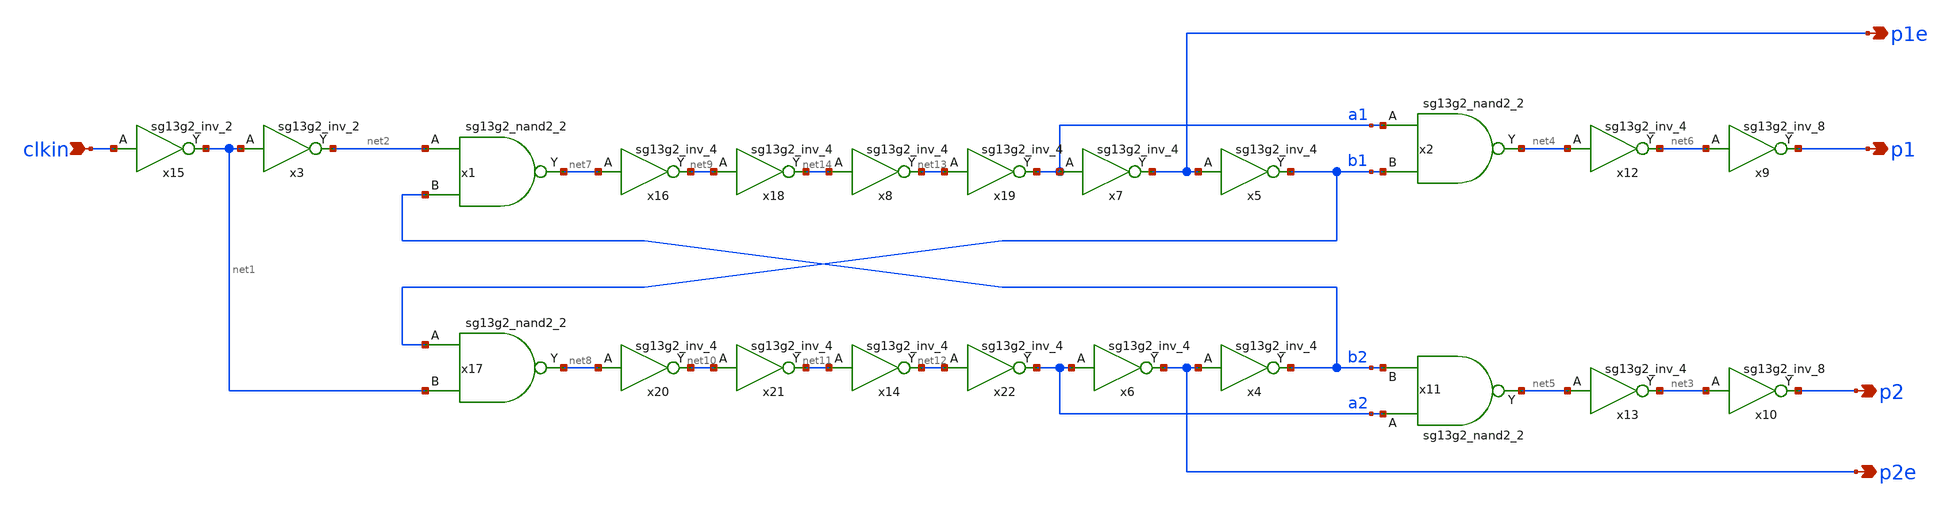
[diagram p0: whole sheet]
** sch_path: 5_Design/4_Layout/Team 4/xschem/clkgen_team4.sch
* IHP-GmbH/IHP-Open-PDK/ihp-sg13g2/libs.tech/xschem/sg13g2_stdcells/sg13g2_inv_2.sch:
* Copyright 2023 IHP PDK Authors
* Licensed under the Apache License, Version 2.0 (the "License");
**.subckt clkgen_team4 p1e p1 p2 p2e clkin
*.opin p1e
*.opin p1
*.opin p2
*.opin p2e
*.ipin clkin
x15 net1 clkin VDD VSS sg13g2_inv_2
x3 net2 net1 VDD VSS sg13g2_inv_2
x17 net8 b1 net1 VDD VSS sg13g2_nand2_2
x1 net7 net2 b2 VDD VSS sg13g2_nand2_2
x2 net4 a1 b1 VDD VSS sg13g2_nand2_2
x11 net5 a2 b2 VDD VSS sg13g2_nand2_2
x12 net6 net4 VDD VSS sg13g2_inv_4
x13 net3 net5 VDD VSS sg13g2_inv_4
x6 p2e a2 VDD VSS sg13g2_inv_4
x4 b2 p2e VDD VSS sg13g2_inv_4
x5 b1 p1e VDD VSS sg13g2_inv_4
x7 p1e a1 VDD VSS sg13g2_inv_4
x8 net13 net14 VDD VSS sg13g2_inv_4
x16 net9 net7 VDD VSS sg13g2_inv_4
x18 net14 net9 VDD VSS sg13g2_inv_4
x19 a1 net13 VDD VSS sg13g2_inv_4
x14 net12 net11 VDD VSS sg13g2_inv_4
x20 net10 net8 VDD VSS sg13g2_inv_4
x21 net11 net10 VDD VSS sg13g2_inv_4
x22 a2 net12 VDD VSS sg13g2_inv_4
x9 p1 net6 VDD VSS sg13g2_inv_8
x10 p2 net3 VDD VSS sg13g2_inv_8
**** begin user architecture code


.param temp=27 vdd=1.2 per=20n
.option method=gear2

.control
save all
tran 10p 15n
set color0=white
plot p1 p2
.endc



.lib /foss/pdks/sg13g2/libs.tech/ngspice/models/cornerMOSlv.lib mos_tt
.lib /foss/pdks/sg13g2/libs.tech/ngspice/models/cornerRES.lib res_typ
.inc /foss/pdks/sg13g2/libs.ref/sg13g2_stdcell/spice/sg13g2_stdcell.spice

**** end user architecture code
**.ends

* expanding   symbol:  sg13g2_stdcells/sg13g2_inv_2.sym # of pins=2
** sym_path: sg13g2_stdcells/sg13g2_inv_2.sym
** sch_path: sg13g2_stdcells/sg13g2_inv_2.sch
.subckt sg13g2_inv_2 Y A VDD VSS
*.opin Y
*.ipin A
*.iopin VDD
*.iopin VSS
XM1 Y A VSS VSS sg13_lv_nmos w=1.48u l=130.00n ng=2 m=1 mm_ok=1
XM2 Y A VDD VDD sg13_lv_pmos w=2.24u l=130.00n ng=2 m=1 mm_ok=1
.ends


* expanding   symbol:  sg13g2_stdcells/sg13g2_nand2_2.sym # of pins=3
** sym_path: sg13g2_stdcells/sg13g2_nand2_2.sym
** sch_path: sg13g2_stdcells/sg13g2_nand2_2.sch
.subckt sg13g2_nand2_2 Y A B VDD VSS
*.iopin VDD
*.iopin VSS
*.opin Y
*.ipin B
*.ipin A
XM1 Y A net1 VSS sg13_lv_nmos w=1.44u l=130.00n ng=2 m=1 mm_ok=1
XM2 net1 B VSS VSS sg13_lv_nmos w=1.44u l=130.00n ng=2 m=1 mm_ok=1
XM3 Y A VDD VDD sg13_lv_pmos w=2.24u l=130.00n ng=2 m=1 mm_ok=1
XM4 Y B VDD VDD sg13_lv_pmos w=2.24u l=130.00n ng=2 m=1 mm_ok=1
.ends


* expanding   symbol:  sg13g2_stdcells/sg13g2_inv_4.sym # of pins=2
** sym_path: sg13g2_stdcells/sg13g2_inv_4.sym
** sch_path: sg13g2_stdcells/sg13g2_inv_4.sch
.subckt sg13g2_inv_4 Y A VDD VSS
*.ipin A
*.opin Y
*.iopin VDD
*.iopin VSS
XM1 Y A VSS VSS sg13_lv_nmos w=2.96u l=130.00n ng=4 m=1 mm_ok=1
XM2 Y A VDD VDD sg13_lv_pmos w=4.48u l=130.00n ng=4 m=1 mm_ok=1
.ends


* expanding   symbol:  sg13g2_stdcells/sg13g2_inv_8.sym # of pins=2
** sym_path: sg13g2_stdcells/sg13g2_inv_8.sym
** sch_path: sg13g2_stdcells/sg13g2_inv_8.sch
.subckt sg13g2_inv_8 Y A VDD VSS
*.opin Y
*.ipin A
*.iopin VDD
*.iopin VSS
XM1 Y A VSS VSS sg13_lv_nmos w=5.92u l=130.00n ng=8 m=1 mm_ok=1
XM2 Y A VDD VDD sg13_lv_pmos w=8.96u l=130.00n ng=8 m=1 mm_ok=1
.ends

.end
